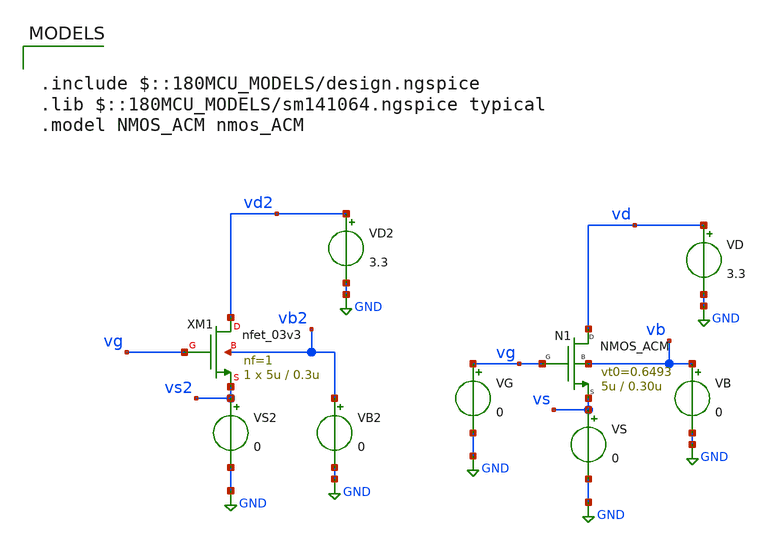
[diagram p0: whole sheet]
** sch_path: Examples/GF180MCU/xschem/TB_nmos_acm.sch
**.subckt TB_nmos_acm
VG vg GND 0
VD vd GND 3.3
VB vb GND 0
VS vs GND 0
N1 vd vg vs vb NMOS_ACM w=5u l=0.30u n=1.383 is=1.076u vt0=0.6493 sigma=26m zeta=22m
VD2 vd2 GND 3.3
VB2 vb2 GND 0
VS2 vs2 GND 0
XM1 vd2 vg vs2 vb2 nfet_03v3 L=0.3u W=5u nf=1 ad='int((nf+1)/2) * W/nf * 0.18u' as='int((nf+2)/2) * W/nf * 0.18u'
+ pd='2*int((nf+1)/2) * (W/nf + 0.18u)' ps='2*int((nf+2)/2) * (W/nf + 0.18u)' nrd='0.18u / W' nrs='0.18u / W'
+ sa=0 sb=0 sd=0 m=1
**** begin user architecture code

.include $::180MCU_MODELS/design.ngspice
.lib $::180MCU_MODELS/sm141064.ngspice typical
.model NMOS_ACM nmos_ACM



.control
pre_osdi /home/gmaranhao/Documents/MOSFET_model/Examples/GF180MCU/xschem/symbol/NMOS_ACM_2V0.osdi
save all

dc VG 0.1 3.3 5m

*gm for ACM
let gm_id = deriv(ln(i(Vs)))

*gm for GF180
let gm_id_gf = deriv(ln(i(Vs2)))

save gm_id gm_id_gf
write TB_nmos_acm.raw

.endc


**** end user architecture code
**.ends
.GLOBAL GND
.end
